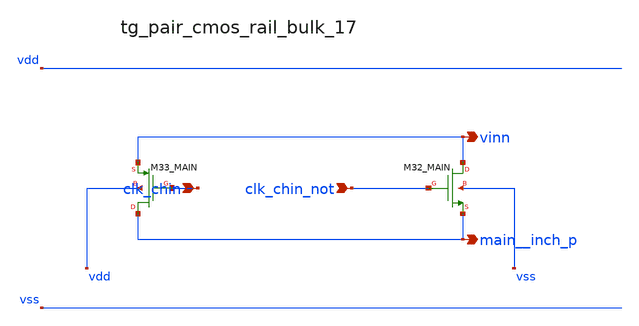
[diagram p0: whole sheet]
** sch_path: analog-db/raw/ia_004_fan_chopper_rrl/hier/blocks/tg_pair_cmos_rail_bulk_17.sch
**.subckt tg_pair_cmos_rail_bulk_17 clk_chin clk_chin_not vinn main__inch_p
*.ipin clk_chin
*.ipin clk_chin_not
*.opin vinn
*.opin main__inch_p
XM32_MAIN vinn clk_chin_not main__inch_p vss sg13_lv_nmos w=x_dut_xm32_main_w l=x_dut_xm32_main_l
+ ng=1 m=x_dut_xm32_main_m
XM33_MAIN main__inch_p clk_chin vinn vdd sg13_lv_pmos w=x_dut_xm33_main_w l=x_dut_xm33_main_l ng=1
+ m=x_dut_xm33_main_m
**.ends
.end
